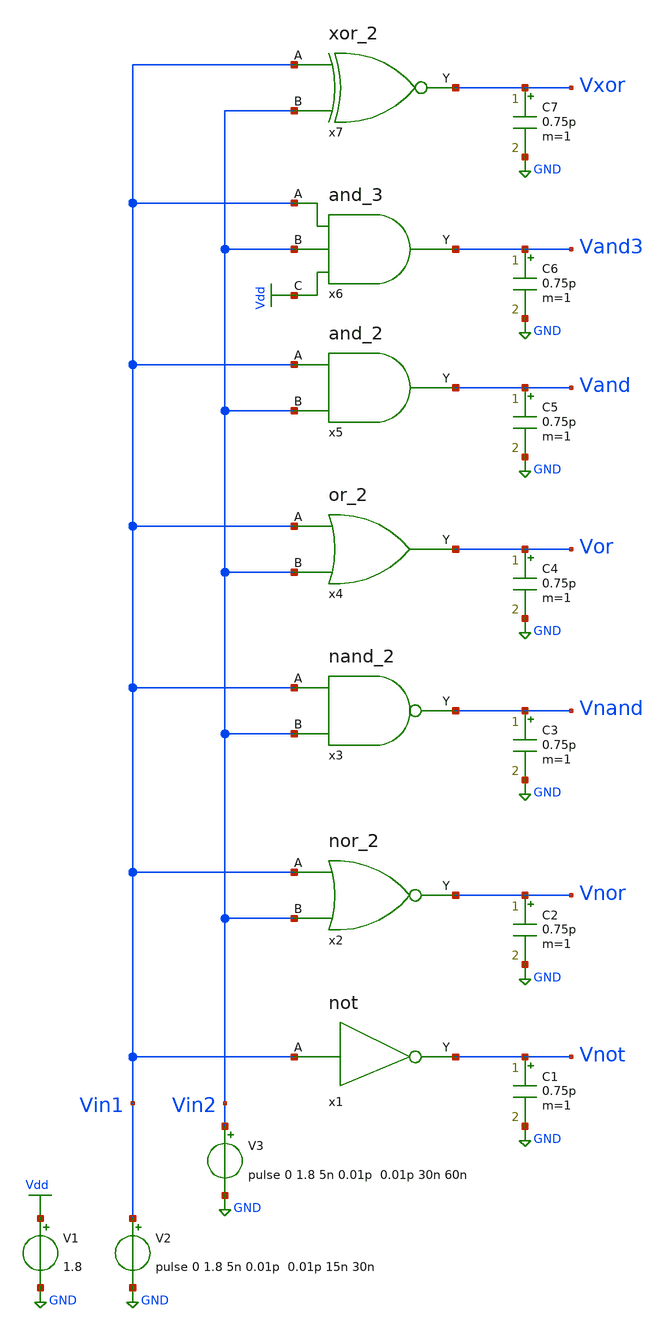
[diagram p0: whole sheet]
** sch_path: Circuiti/logic-gates.sch
**.subckt logic-gates
V1 Vdd GND 1.8
V2 Vin1 GND pulse 0 1.8 5n 0.01p 0.01p 15n 30n
V3 Vin2 GND pulse 0 1.8 5n 0.01p 0.01p 30n 60n
x1 Vin1 Vnot not
x2 Vin1 Vnor Vin2 nor_2
x3 Vin1 Vnand Vin2 nand_2
x4 Vin1 Vor Vin2 or_2
x5 Vin1 Vand Vin2 and_2
x6 Vin1 Vand3 Vin2 Vdd and_3
C1 Vnot GND 0.75p m=1
C2 Vnor GND 0.75p m=1
C3 Vnand GND 0.75p m=1
C4 Vor GND 0.75p m=1
C5 Vand GND 0.75p m=1
C6 Vand3 GND 0.75p m=1
x7 Vin1 Vxor Vin2 xor_2
C7 Vxor GND 0.75p m=1
**** begin user architecture code


.lib /home/matteo/xschem_downloads/skywater-pdk/libraries/sky130_fd_pr_ngspice/latest/models/sky130.lib.spice tt

*.include /home/matteo/xschem_downloads/skywater-pdk/libraries/sky130_fd_pr_ngspice/latest/cells/nfet_01v8/sky130_fd_pr__nfet_01v8__tt.corner.spice

.param mc_mm_switch=0
.param mc_pr_switch=1


 .control
tran 0.1n 90n
plot vin1 vin2+2 vnot+4 vnor+6 vnand+8 vor+10 vand+12 vand3+14 vxor+16
plot vin1 vin2+2 vxor+4
wrdata output.txt vin1 vin2 vnot vnor vnand vor vnand vxor
.endc

**** end user architecture code
**.ends

* expanding   symbol:  /home/matteo/Documenti/tesi/Circuiti/logic_gates_sch_sym/not.sym # of pins=2
** sym_path: Circuiti/logic_gates_sch_sym/not.sym
** sch_path: Circuiti/logic_gates_sch_sym/not.sch
.subckt not A Y
*.ipin A
*.opin Y
XM1 Y A GND GND sky130_fd_pr__nfet_01v8 L=0.45 W=1 nf=1 ad='int((nf+1)/2) * W/nf * 0.29' as='int((nf+2)/2) * W/nf * 0.29'
+ pd='2*int((nf+1)/2) * (W/nf + 0.29)' ps='2*int((nf+2)/2) * (W/nf + 0.29)' nrd='0.29 / W' nrs='0.29 / W'
+ sa=0 sb=0 sd=0 mult=1 m=1
XM2 Y A Vdd VDD sky130_fd_pr__pfet_01v8 L=0.45 W=4.8 nf=1 ad='int((nf+1)/2) * W/nf * 0.29' as='int((nf+2)/2) * W/nf * 0.29'
+ pd='2*int((nf+1)/2) * (W/nf + 0.29)' ps='2*int((nf+2)/2) * (W/nf + 0.29)' nrd='0.29 / W' nrs='0.29 / W'
+ sa=0 sb=0 sd=0 mult=1 m=1
.ends


* expanding   symbol:  /home/matteo/Documenti/tesi/Circuiti/logic_gates_sch_sym/nor_2.sym # of
*+ pins=3
** sym_path: Circuiti/logic_gates_sch_sym/nor_2.sym
** sch_path: Circuiti/logic_gates_sch_sym/nor_2.sch
.subckt nor_2 A Y B
*.opin Y
*.ipin A
*.ipin B
XM1 Y B GND GND sky130_fd_pr__nfet_01v8 L=0.45 W=1 nf=1 ad='int((nf+1)/2) * W/nf * 0.29' as='int((nf+2)/2) * W/nf * 0.29'
+ pd='2*int((nf+1)/2) * (W/nf + 0.29)' ps='2*int((nf+2)/2) * (W/nf + 0.29)' nrd='0.29 / W' nrs='0.29 / W'
+ sa=0 sb=0 sd=0 mult=1 m=1
XM3 Y B net1 VDD sky130_fd_pr__pfet_01v8 L=0.15 W=4.8 nf=1 ad='int((nf+1)/2) * W/nf * 0.29' as='int((nf+2)/2) * W/nf * 0.29'
+ pd='2*int((nf+1)/2) * (W/nf + 0.29)' ps='2*int((nf+2)/2) * (W/nf + 0.29)' nrd='0.29 / W' nrs='0.29 / W'
+ sa=0 sb=0 sd=0 mult=1 m=1
XM4 net1 A Vdd VDD sky130_fd_pr__pfet_01v8 L=0.15 W=4.8 nf=1 ad='int((nf+1)/2) * W/nf * 0.29' as='int((nf+2)/2) * W/nf * 0.29'
+ pd='2*int((nf+1)/2) * (W/nf + 0.29)' ps='2*int((nf+2)/2) * (W/nf + 0.29)' nrd='0.29 / W' nrs='0.29 / W'
+ sa=0 sb=0 sd=0 mult=1 m=1
XM2 Y A GND GND sky130_fd_pr__nfet_01v8 L=0.45 W=1 nf=1 ad='int((nf+1)/2) * W/nf * 0.29' as='int((nf+2)/2) * W/nf * 0.29'
+ pd='2*int((nf+1)/2) * (W/nf + 0.29)' ps='2*int((nf+2)/2) * (W/nf + 0.29)' nrd='0.29 / W' nrs='0.29 / W'
+ sa=0 sb=0 sd=0 mult=1 m=1
.ends


* expanding   symbol:  /home/matteo/Documenti/tesi/Circuiti/logic_gates_sch_sym/nand_2.sym # of
*+ pins=3
** sym_path: Circuiti/logic_gates_sch_sym/nand_2.sym
** sch_path: Circuiti/logic_gates_sch_sym/nand_2.sch
.subckt nand_2 A Y B
*.ipin A
*.ipin B
*.opin Y
XM1 Y A net1 GND sky130_fd_pr__nfet_01v8 L=0.15 W=1 nf=1 ad='int((nf+1)/2) * W/nf * 0.29' as='int((nf+2)/2) * W/nf * 0.29'
+ pd='2*int((nf+1)/2) * (W/nf + 0.29)' ps='2*int((nf+2)/2) * (W/nf + 0.29)' nrd='0.29 / W' nrs='0.29 / W'
+ sa=0 sb=0 sd=0 mult=1 m=1
XM3 Y B Vdd VDD sky130_fd_pr__pfet_01v8 L=0.45 W=4.8 nf=1 ad='int((nf+1)/2) * W/nf * 0.29' as='int((nf+2)/2) * W/nf * 0.29'
+ pd='2*int((nf+1)/2) * (W/nf + 0.29)' ps='2*int((nf+2)/2) * (W/nf + 0.29)' nrd='0.29 / W' nrs='0.29 / W'
+ sa=0 sb=0 sd=0 mult=1 m=1
XM4 Y A Vdd VDD sky130_fd_pr__pfet_01v8 L=0.45 W=4.8 nf=1 ad='int((nf+1)/2) * W/nf * 0.29' as='int((nf+2)/2) * W/nf * 0.29'
+ pd='2*int((nf+1)/2) * (W/nf + 0.29)' ps='2*int((nf+2)/2) * (W/nf + 0.29)' nrd='0.29 / W' nrs='0.29 / W'
+ sa=0 sb=0 sd=0 mult=1 m=1
XM2 net1 B GND GND sky130_fd_pr__nfet_01v8 L=0.15 W=1 nf=1 ad='int((nf+1)/2) * W/nf * 0.29' as='int((nf+2)/2) * W/nf * 0.29'
+ pd='2*int((nf+1)/2) * (W/nf + 0.29)' ps='2*int((nf+2)/2) * (W/nf + 0.29)' nrd='0.29 / W' nrs='0.29 / W'
+ sa=0 sb=0 sd=0 mult=1 m=1
.ends


* expanding   symbol:  /home/matteo/Documenti/tesi/Circuiti/logic_gates_sch_sym/or_2.sym # of pins=3
** sym_path: Circuiti/logic_gates_sch_sym/or_2.sym
** sch_path: Circuiti/logic_gates_sch_sym/or_2.sch
.subckt or_2 A Y B
*.ipin A
*.ipin B
*.opin Y
x1 A net1 B nor_2
x2 net1 Y not
.ends


* expanding   symbol:  /home/matteo/Documenti/tesi/Circuiti/logic_gates_sch_sym/and_2.sym # of
*+ pins=3
** sym_path: Circuiti/logic_gates_sch_sym/and_2.sym
** sch_path: Circuiti/logic_gates_sch_sym/and_2.sch
.subckt and_2 A Y B
*.ipin B
*.ipin A
*.opin Y
x1 A net1 B nand_2
x2 net1 Y not
.ends


* expanding   symbol:  /home/matteo/Documenti/tesi/Circuiti/logic_gates_sch_sym/and_3.sym # of
*+ pins=4
** sym_path: Circuiti/logic_gates_sch_sym/and_3.sym
** sch_path: Circuiti/logic_gates_sch_sym/and_3.sch
.subckt and_3 A Y B C
*.ipin A
*.ipin B
*.ipin C
*.opin Y
x1 A Y net1 and_2
x2 B net1 C and_2
.ends


* expanding   symbol:  /home/matteo/Documenti/tesi/Circuiti/logic_gates_sch_sym/xor_2.sym # of
*+ pins=3
** sym_path: Circuiti/logic_gates_sch_sym/xor_2.sym
** sch_path: Circuiti/logic_gates_sch_sym/xor_2.sch
.subckt xor_2 A Y B
*.ipin A
*.ipin B
*.opin Y
x1 A net1 B nand_2
x2 A net2 B or_2
x3 net1 Y net2 and_2
.ends

.GLOBAL GND
.GLOBAL Vdd
.end
